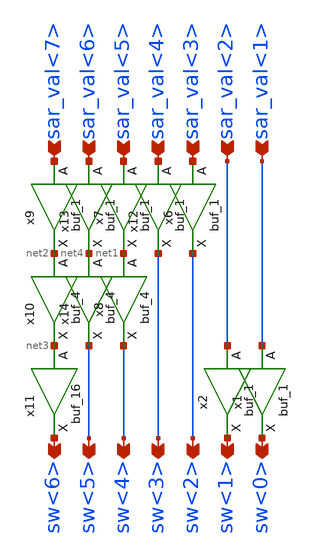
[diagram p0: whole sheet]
** sch_path: hgu/xschem/hgu_cdac_sw_buffer.sch
**.subckt hgu_cdac_sw_buffer sar_val<7> sw<6> sw<5> sw<4> sw<3> sw<2> sw<1> sw<0> sar_val<6>
*+ sar_val<5> sar_val<4> sar_val<3> sar_val<2> sar_val<1>
*.ipin sar_val<7>
*.opin sw<6>
*.opin sw<5>
*.opin sw<4>
*.opin sw<3>
*.opin sw<2>
*.opin sw<1>
*.opin sw<0>
*.ipin sar_val<6>
*.ipin sar_val<5>
*.ipin sar_val<4>
*.ipin sar_val<3>
*.ipin sar_val<2>
*.ipin sar_val<1>
x6 sar_val<3> VGND VNB VPB VPWR sw<2> sky130_fd_sc_hd__buf_1
x7 sar_val<5> VGND VNB VPB VPWR net1 sky130_fd_sc_hd__buf_1
x9 sar_val<7> VGND VNB VPB VPWR net2 sky130_fd_sc_hd__buf_1
x8 net1 VGND VNB VPB VPWR sw<4> sky130_fd_sc_hd__buf_4
x10 net2 VGND VNB VPB VPWR net3 sky130_fd_sc_hd__buf_4
x11 net3 VGND VNB VPB VPWR sw<6> sky130_fd_sc_hd__buf_16
x12 sar_val<4> VGND VNB VPB VPWR sw<3> sky130_fd_sc_hd__buf_1
x13 sar_val<6> VGND VNB VPB VPWR net4 sky130_fd_sc_hd__buf_1
x14 net4 VGND VNB VPB VPWR sw<5> sky130_fd_sc_hd__buf_4
x1 sar_val<1> VGND VNB VPB VPWR sw<0> sky130_fd_sc_hd__buf_1
x2 sar_val<2> VGND VNB VPB VPWR sw<1> sky130_fd_sc_hd__buf_1
**.ends
.end
